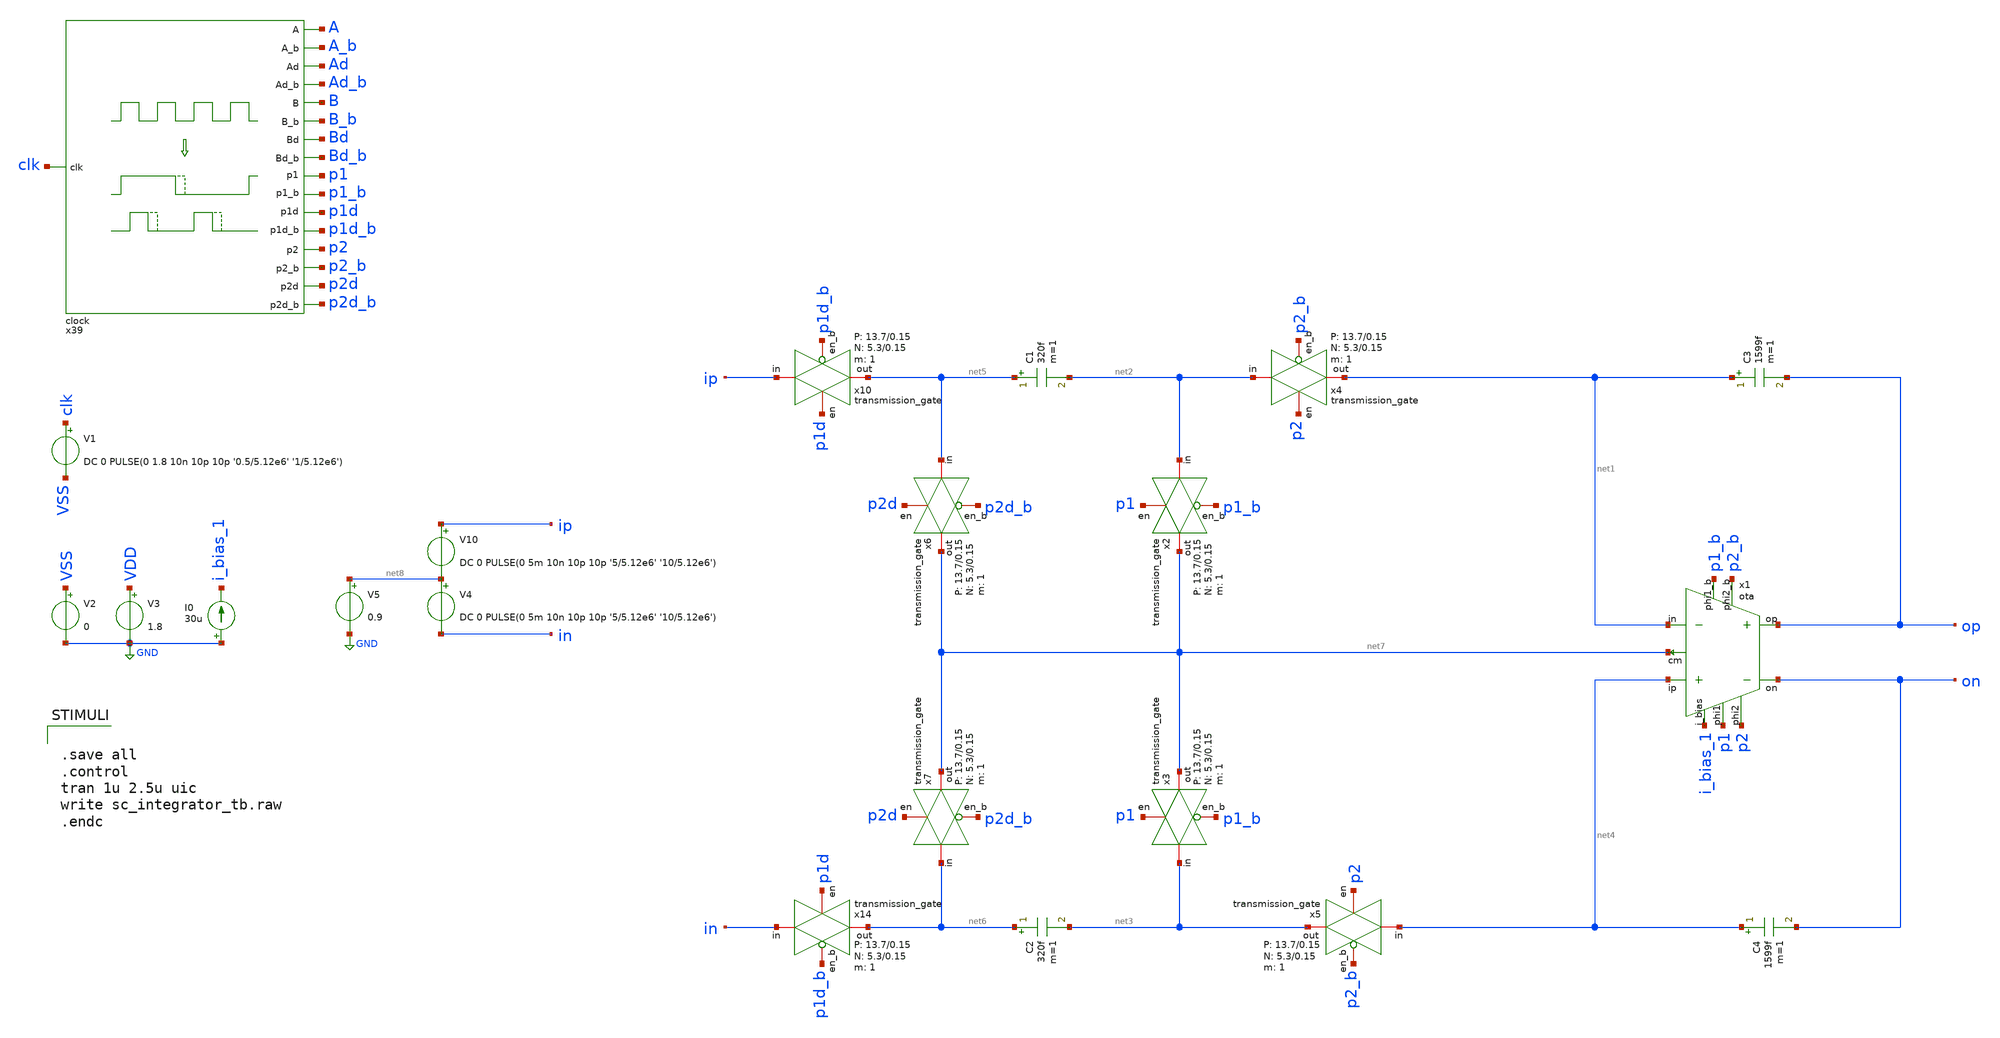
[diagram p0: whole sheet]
** sch_path: verification/schematic/sc_integrator_tb.sch
**.subckt sc_integrator_tb
x1 i_bias_1 net4 net1 p1 p1_b p2 p2_b op on net7 50 350 VDD VSS ota
x4 net2 net1 p2 p2_b VDD VSS 1 5.3 0.15 13.7 0.15 transmission_gate
x5 net4 net3 p2 p2_b VDD VSS 1 5.3 0.15 13.7 0.15 transmission_gate
x2 net2 net7 p1 p1_b VDD VSS 1 5.3 0.15 13.7 0.15 transmission_gate
x3 net3 net7 p1 p1_b VDD VSS 1 5.3 0.15 13.7 0.15 transmission_gate
C1 net5 net2 320f m=1
C2 net6 net3 320f m=1
x10 ip net5 p1d p1d_b VDD VSS 1 5.3 0.15 13.7 0.15 transmission_gate
x14 in net6 p1d p1d_b VDD VSS 1 5.3 0.15 13.7 0.15 transmission_gate
C3 net1 op 1599f m=1
C4 net4 on 1599f m=1
x39 A A_b Ad Ad_b Bd_b Bd B_b B p2 p2_b p2d clk p2d_b p1d_b p1d p1_b p1 VDD VSS clock
V1 clk VSS DC 0 PULSE(0 1.8 10n 10p 10p '0.5/5.12e6' '1/5.12e6')
V2 VSS GND 0
V3 VDD GND 1.8
I0 GND i_bias_1 30u
x6 net5 net7 p2d p2d_b VDD VSS 1 5.3 0.15 13.7 0.15 transmission_gate
x7 net6 net7 p2d p2d_b VDD VSS 1 5.3 0.15 13.7 0.15 transmission_gate
V10 ip net8 DC 0 PULSE(0 5m 10n 10p 10p '5/5.12e6' '10/5.12e6')
V4 net8 in DC 0 PULSE(0 5m 10n 10p 10p '5/5.12e6' '10/5.12e6')
V5 net8 GND 0.9
**** begin user architecture code

** opencircuitdesign pdks install
.lib /farmshare/home/classes/ee/372/PDKs/open_pdks_1.0.310/sky130/sky130A/libs.tech/ngspice/sky130.lib.spice tt
.inc /farmshare/home/classes/ee/372/PDKs/open_pdks_1.0.310/sky130/sky130A/libs.ref/sky130_fd_sc_hd/spice/sky130_fd_sc_hd.spice



.save all
.control
tran 1u 2.5u uic
write sc_integrator_tb.raw
.endc


**** end user architecture code
**.ends
.GLOBAL GND
.end
